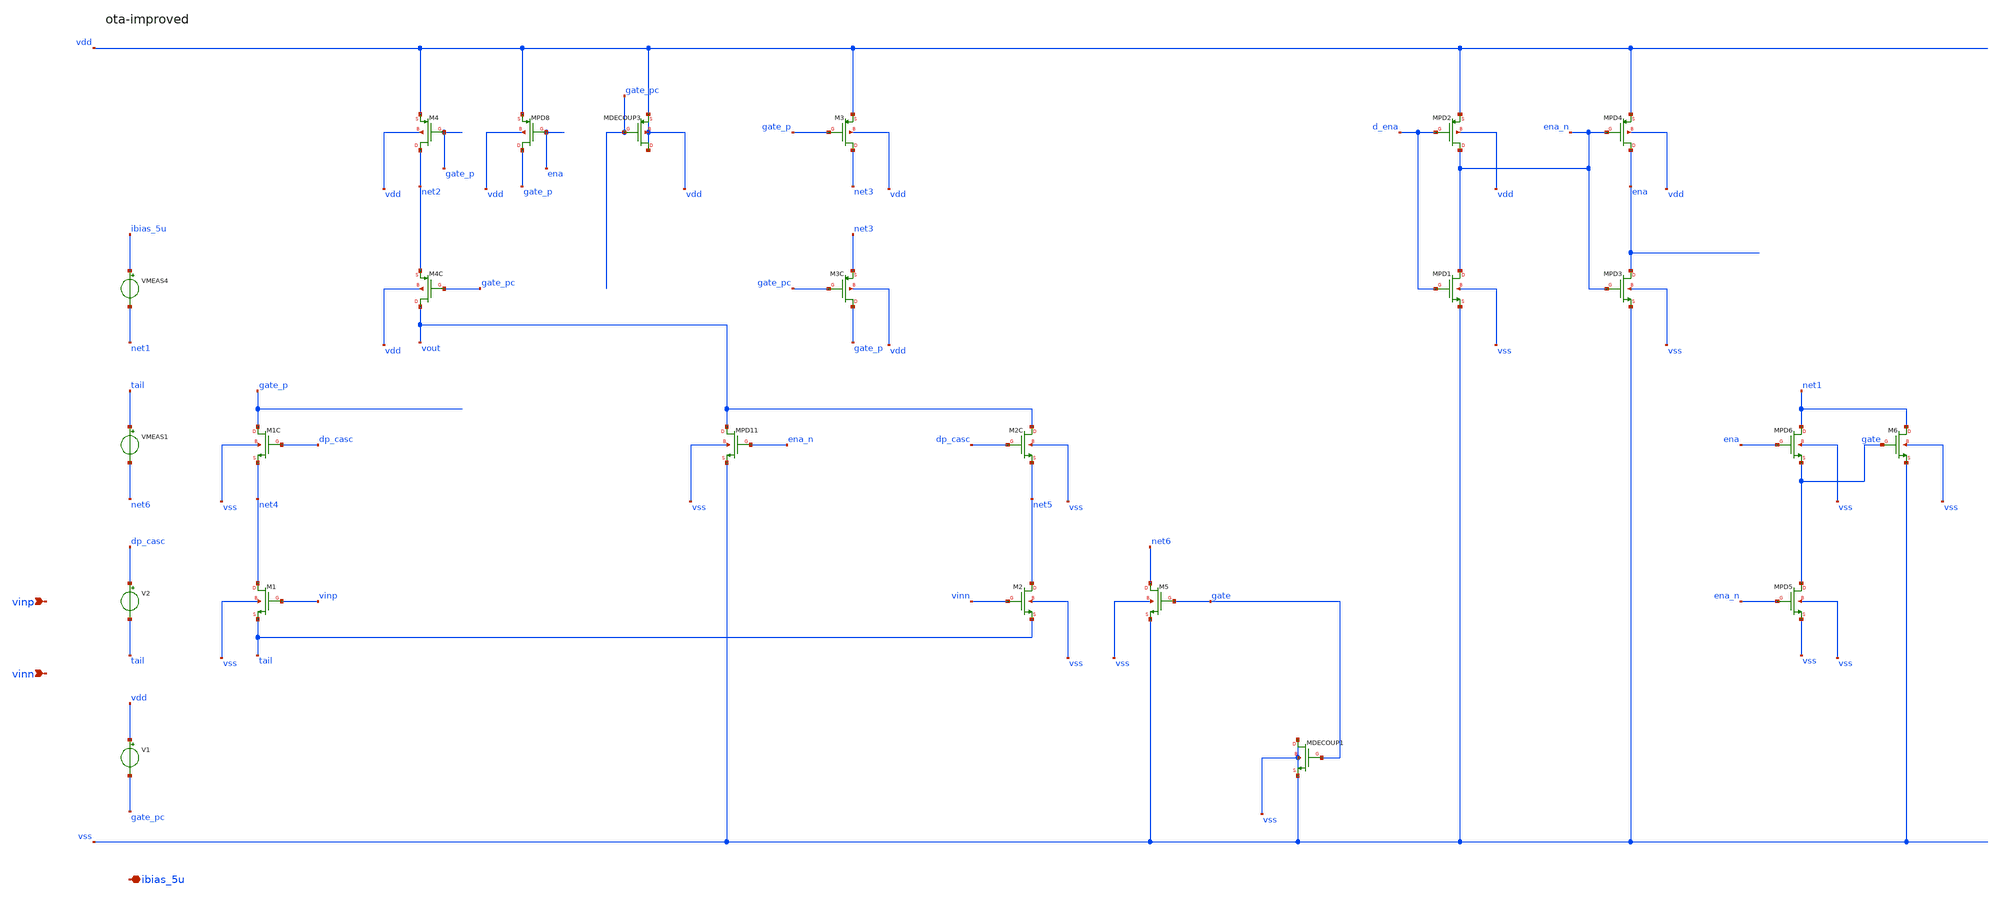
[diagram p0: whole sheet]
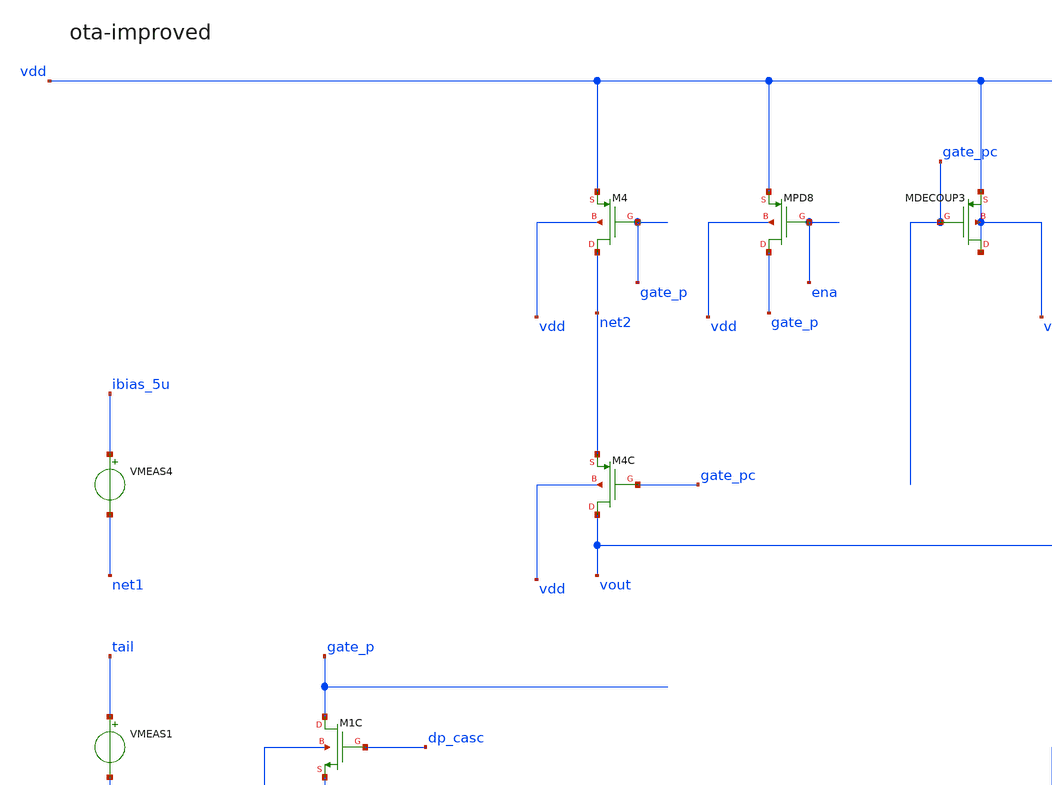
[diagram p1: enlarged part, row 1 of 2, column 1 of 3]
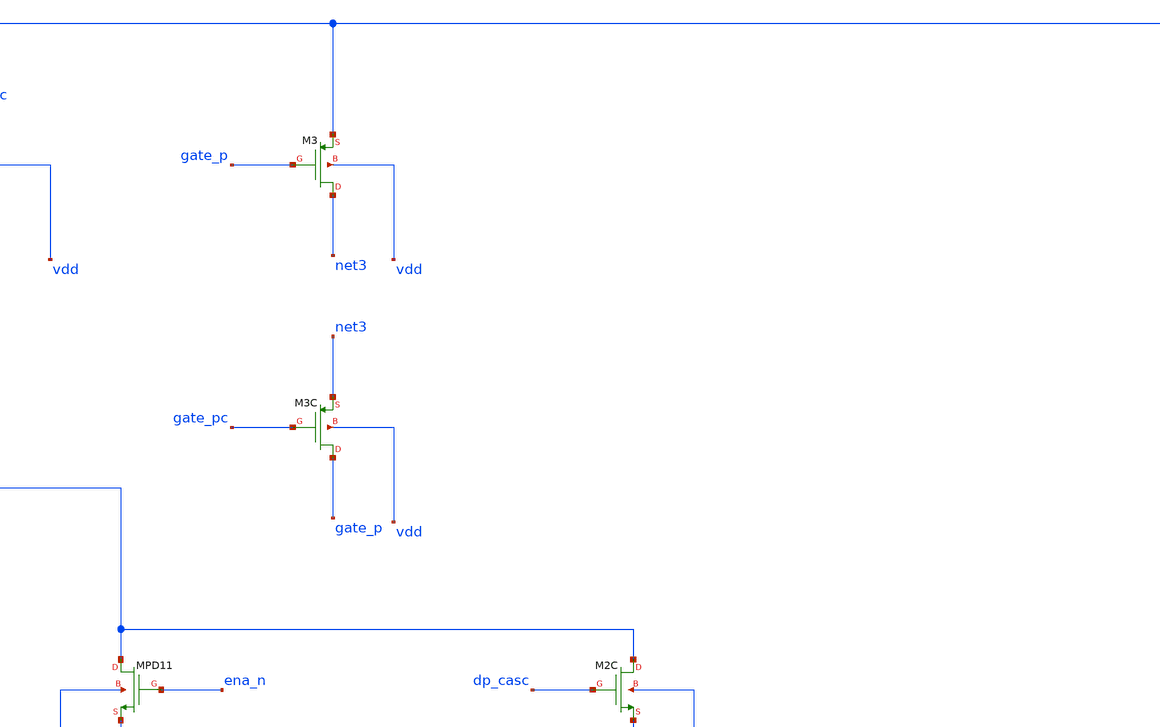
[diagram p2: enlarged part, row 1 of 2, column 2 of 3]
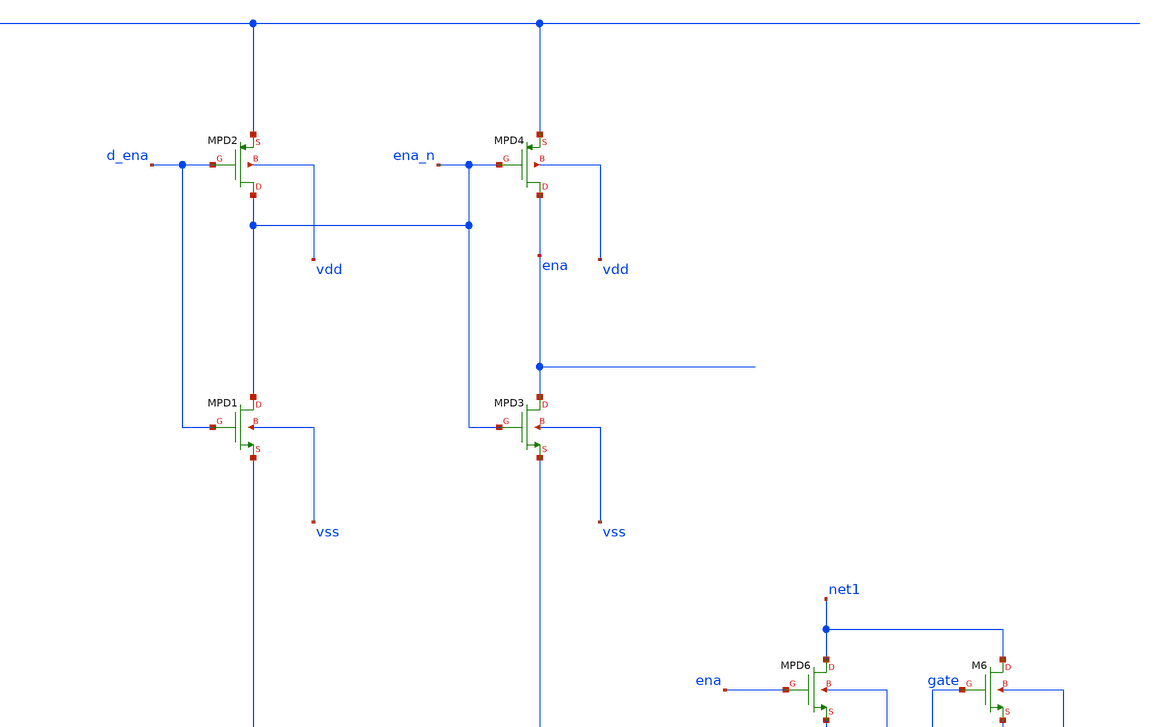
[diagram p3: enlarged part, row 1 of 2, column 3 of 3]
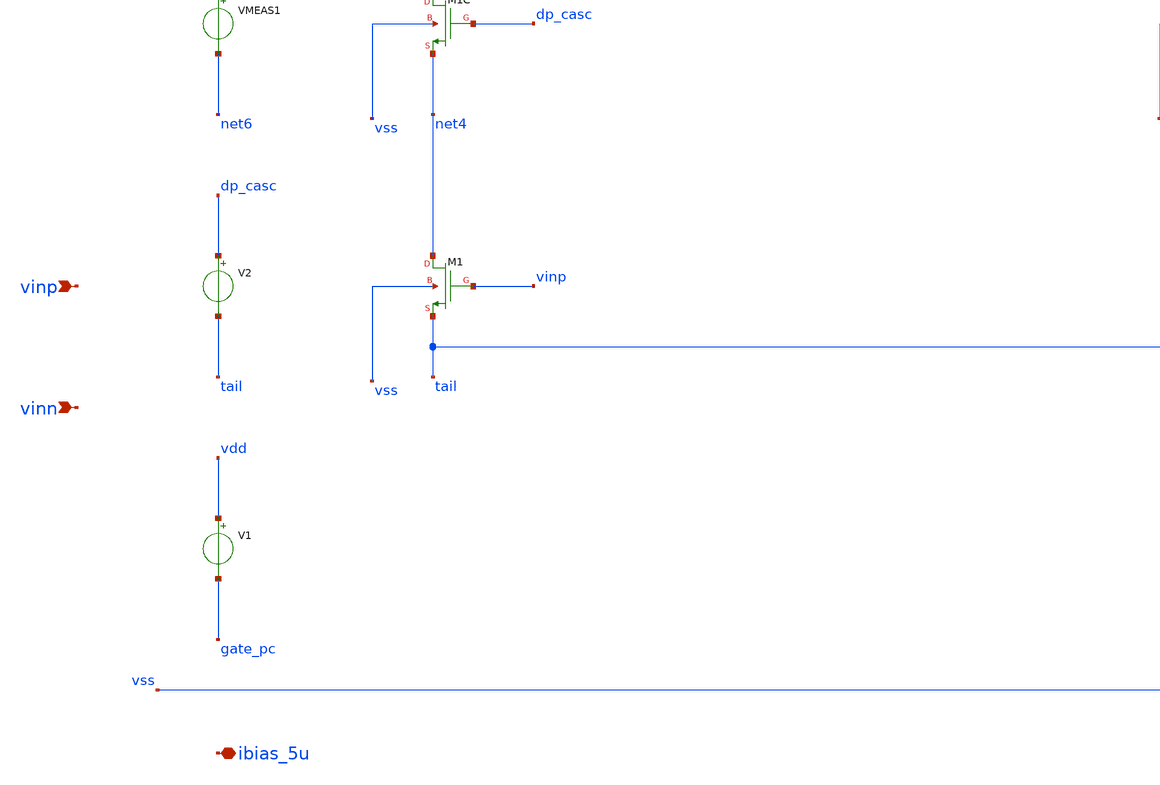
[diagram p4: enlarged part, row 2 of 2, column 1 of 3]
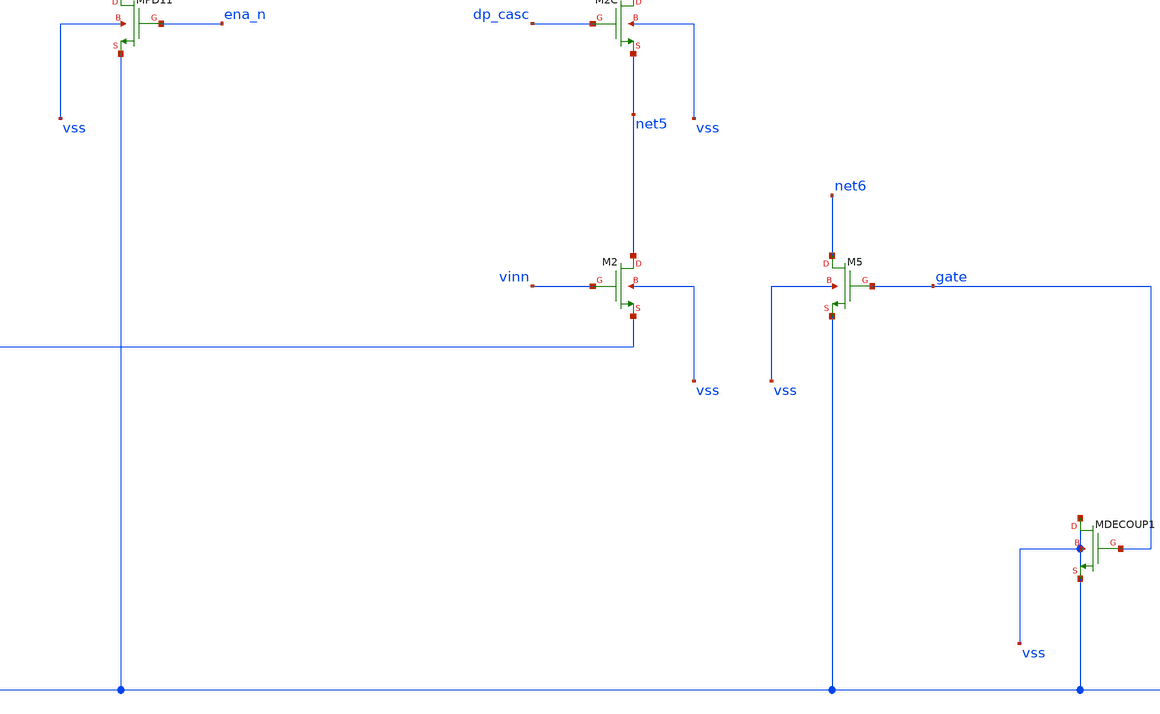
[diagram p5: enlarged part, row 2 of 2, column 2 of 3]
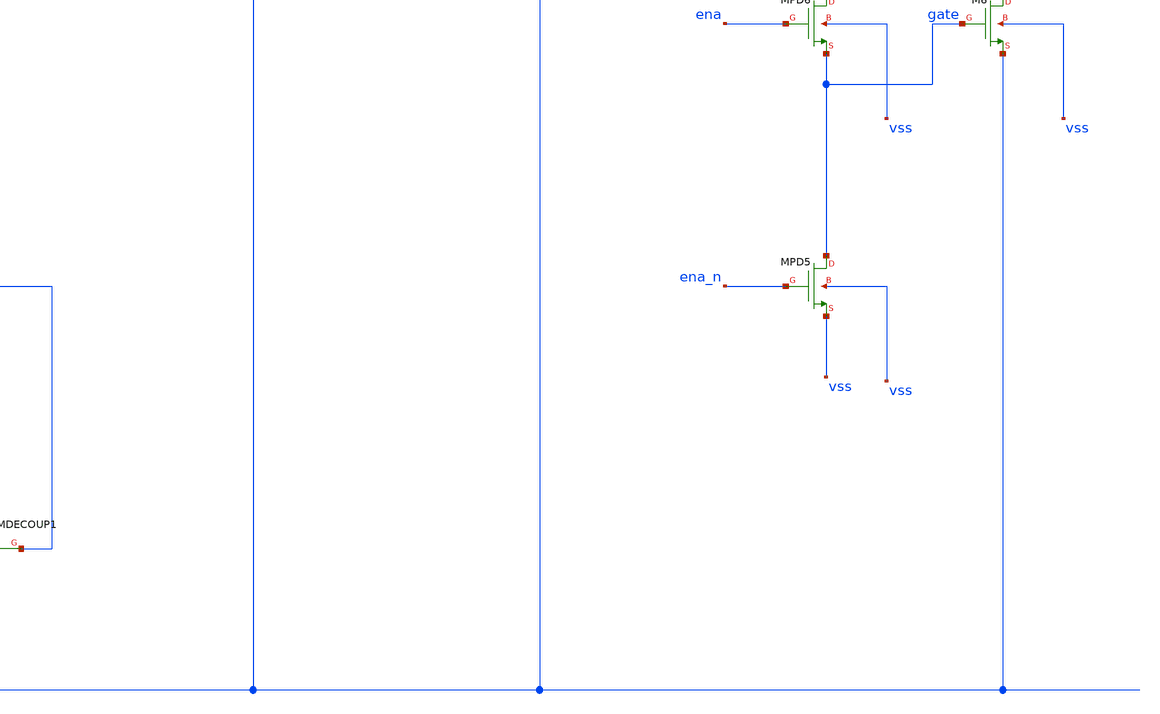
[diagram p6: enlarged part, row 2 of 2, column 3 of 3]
** sch_path: platform/packages/spicexplorer-netlist2xschem/notebooks/ota-improved.sch
**.subckt ota-improved vinp vinn ibias_5u
*.ipin vinp
*.ipin vinn
*.iopin ibias_5u
XM5 net6 gate vss vss sg13_lv_nmos w=X_DUT_M5_W l=X_DUT_M5_L ng=X_DUT_M5_NG m=1
XM4 net2 gate_p vdd vdd sg13_lv_pmos w=X_DUT_M3M4_W l=X_DUT_M3M4_L ng=1 m=1
XM1 net4 vinp tail vss sg13_lv_nmos w=X_DUT_M1M2_W l=X_DUT_M1M2_L ng=1 m=1
XM2 net5 vinn tail vss sg13_lv_nmos w=X_DUT_M1M2_W l=X_DUT_M1M2_L ng=1 m=1
XM3 net3 gate_p vdd vdd sg13_lv_pmos w=X_DUT_M3M4_W l=X_DUT_M3M4_L ng=1 m=1
XM6 net1 gate vss vss sg13_lv_nmos w=X_DUT_M6_W l=X_DUT_M6_L ng=1 m=1
XMPD5 gate ena_n vss vss sg13_lv_nmos w=1u l=0.13u ng=1 m=1
XMPD3 ena ena_n vss vss sg13_lv_nmos w=1u l=0.13u ng=1 m=1
XMPD4 ena ena_n vdd vdd sg13_lv_pmos w=1u l=0.13u ng=1 m=1
XMPD6 net1 ena gate vss sg13_lv_nmos w=1u l=0.13u ng=1 m=1
XM2C vout dp_casc net5 vss sg13_lv_nmos w=X_DUT_M1CM2C_W l=X_DUT_M1CM2C_L ng=1 m=1
XM1C gate_p dp_casc net4 vss sg13_lv_nmos w=X_DUT_M1CM2C_W l=X_DUT_M1CM2C_L ng=1 m=1
XM4C vout gate_pc net2 vdd sg13_lv_pmos w=X_DUT_M3CM4C_W l=X_DUT_M3PCM4C_L ng=1 m=1
XM3C gate_p gate_pc net3 vdd sg13_lv_pmos w=X_DUT_M3CM4C_W l=X_DUT_M3CM4C_L ng=1 m=1
XMPD8 gate_p ena vdd vdd sg13_lv_pmos w=1u l=0.13u ng=1 m=1
VMEAS1 tail net6 0
XMPD1 ena_n d_ena vss vss sg13_lv_nmos w=1u l=0.13u ng=1 m=1
XMPD2 ena_n d_ena vdd vdd sg13_lv_pmos w=1u l=0.13u ng=1 m=1
VMEAS4 ibias_5u net1 0P
XMPD11 vout ena_n vss vss sg13_lv_nmos w=0.5u l=0.13u ng=1 m=1
XMDECOUP1 vss gate vss vss sg13_lv_nmos w=8u l=1u ng=4 m=1
XMDECOUP3 vdd gate_pc vdd vdd sg13_lv_pmos w=12u l=0.5u ng=4 m=1
V1 vdd gate_pc X_DUT_V_BIAS_2
V2 dp_casc tail X_DUT_V_BIAS_1
**.ends
.end
